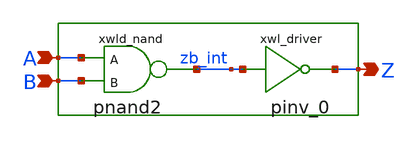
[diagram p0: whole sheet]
** sch_path: sram_2_64_scn4m_lcc/wordline_driver.sch
**.subckt wordline_driver A B Z
*.ipin A
*.ipin B
*.opin Z
xwld_nand A B zb_int vdd gnd pnand2
xwl_driver zb_int Z vdd gnd pinv_0
**.ends
.end
